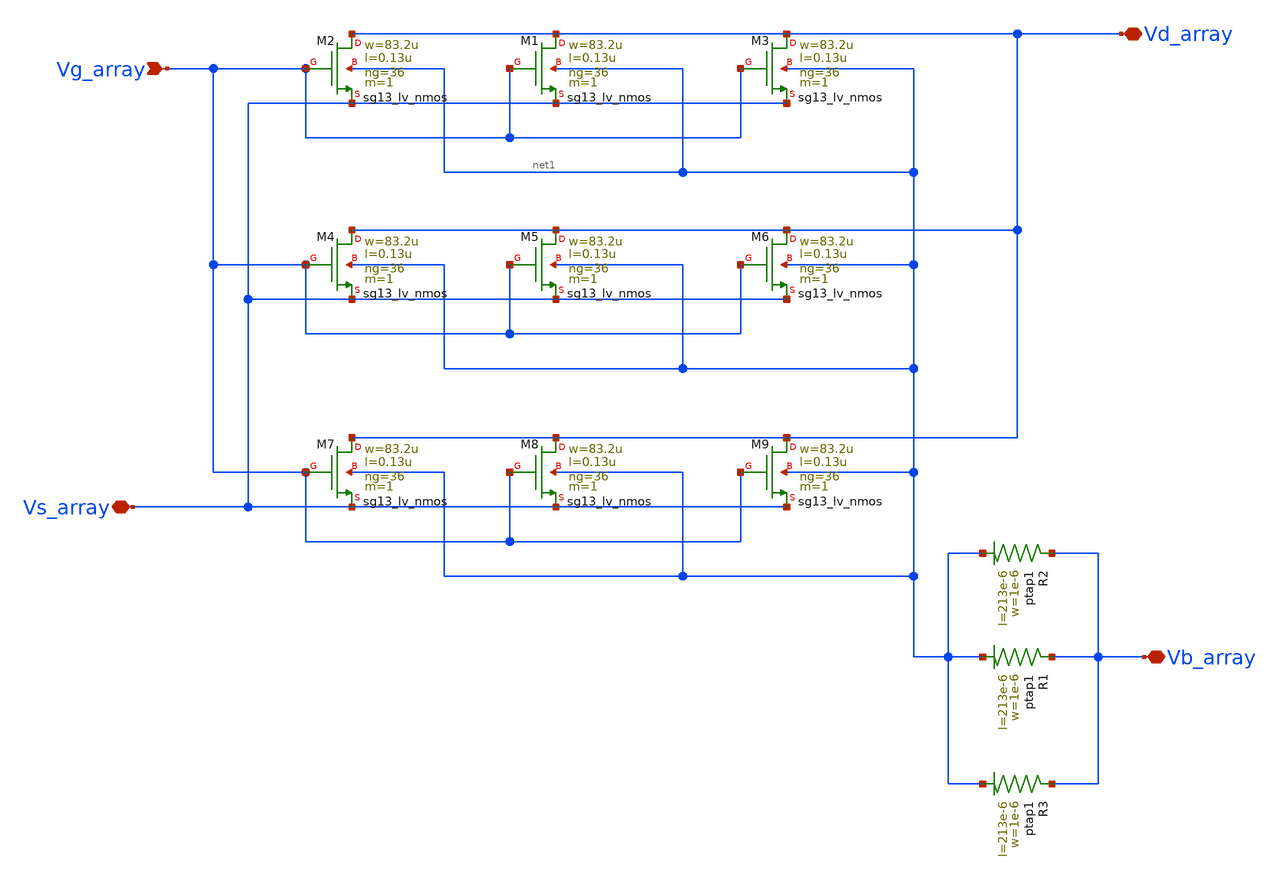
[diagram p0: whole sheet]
** sch_path: untitled-12.sch
**.subckt untitled-12 Vd_array Vg_array Vs_array Vb_array
*.iopin Vd_array
*.ipin Vg_array
*.iopin Vs_array
*.iopin Vb_array
XM2 Vd_array Vg_array Vs_array net1 sg13_lv_nmos w=83.2u l=0.13u ng=36 m=1 mm_ok=1
XM1 Vd_array Vg_array Vs_array net1 sg13_lv_nmos w=83.2u l=0.13u ng=36 m=1 mm_ok=1
XM3 Vd_array Vg_array Vs_array net1 sg13_lv_nmos w=83.2u l=0.13u ng=36 m=1 mm_ok=1
XM4 Vd_array Vg_array Vs_array net1 sg13_lv_nmos w=83.2u l=0.13u ng=36 m=1 mm_ok=1
XM5 Vd_array Vg_array Vs_array net1 sg13_lv_nmos w=83.2u l=0.13u ng=36 m=1 mm_ok=1
XM6 Vd_array Vg_array Vs_array net1 sg13_lv_nmos w=83.2u l=0.13u ng=36 m=1 mm_ok=1
XM7 Vd_array Vg_array Vs_array net1 sg13_lv_nmos w=83.2u l=0.13u ng=36 m=1 mm_ok=1
XM8 Vd_array Vg_array Vs_array net1 sg13_lv_nmos w=83.2u l=0.13u ng=36 m=1 mm_ok=1
XM9 Vd_array Vg_array Vs_array net1 sg13_lv_nmos w=83.2u l=0.13u ng=36 m=1 mm_ok=1
XR1 Vb_array net1 ptap1 R=1.529 w=1e-6 l=213e-6
XR2 Vb_array net1 ptap1 R=1.529 w=1e-6 l=213e-6
XR3 Vb_array net1 ptap1 R=1.529 w=1e-6 l=213e-6
**.ends
.end
